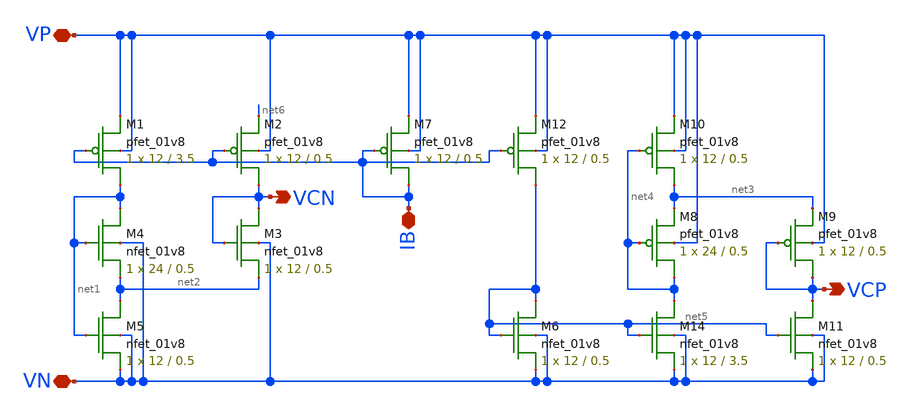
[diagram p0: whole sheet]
** sch_path: mp3/schematics/bias_generator (another copy).sch
**.subckt bias_generator (another copy) VCN VP VN VCP IB
*.opin VCN
*.iopin VP
*.iopin VN
*.opin VCP
*.iopin IB
XM1 net1 IB VP VP sky130_fd_pr__pfet_01v8 L=3.5 W=12 nf=1 ad='int((nf+1)/2) * W/nf * 0.29' as='int((nf+2)/2) * W/nf * 0.29'
+ pd='2*int((nf+1)/2) * (W/nf + 0.29)' ps='2*int((nf+2)/2) * (W/nf + 0.29)' nrd='0.29 / W' nrs='0.29 / W'
+ sa=0 sb=0 sd=0 mult=1 m=1
XM2 VCN IB net6 VP sky130_fd_pr__pfet_01v8 L=0.5 W=12 nf=1 ad='int((nf+1)/2) * W/nf * 0.29' as='int((nf+2)/2) * W/nf * 0.29'
+ pd='2*int((nf+1)/2) * (W/nf + 0.29)' ps='2*int((nf+2)/2) * (W/nf + 0.29)' nrd='0.29 / W' nrs='0.29 / W'
+ sa=0 sb=0 sd=0 mult=1 m=1
XM8 net4 net4 net3 VP sky130_fd_pr__pfet_01v8 L=0.5 W=24 nf=1 ad='int((nf+1)/2) * W/nf * 0.29' as='int((nf+2)/2) * W/nf * 0.29'
+ pd='2*int((nf+1)/2) * (W/nf + 0.29)' ps='2*int((nf+2)/2) * (W/nf + 0.29)' nrd='0.29 / W' nrs='0.29 / W'
+ sa=0 sb=0 sd=0 mult=1 m=1
XM9 VCP VCP net3 VP sky130_fd_pr__pfet_01v8 L=0.5 W=12 nf=1 ad='int((nf+1)/2) * W/nf * 0.29' as='int((nf+2)/2) * W/nf * 0.29'
+ pd='2*int((nf+1)/2) * (W/nf + 0.29)' ps='2*int((nf+2)/2) * (W/nf + 0.29)' nrd='0.29 / W' nrs='0.29 / W'
+ sa=0 sb=0 sd=0 mult=1 m=1
XM10 net3 net4 VP VP sky130_fd_pr__pfet_01v8 L=0.5 W=12 nf=1 ad='int((nf+1)/2) * W/nf * 0.29' as='int((nf+2)/2) * W/nf * 0.29'
+ pd='2*int((nf+1)/2) * (W/nf + 0.29)' ps='2*int((nf+2)/2) * (W/nf + 0.29)' nrd='0.29 / W' nrs='0.29 / W'
+ sa=0 sb=0 sd=0 mult=1 m=1
XM11 VCP net5 VN VN sky130_fd_pr__nfet_01v8 L=0.5 W=12 nf=1 ad='int((nf+1)/2) * W/nf * 0.29' as='int((nf+2)/2) * W/nf * 0.29'
+ pd='2*int((nf+1)/2) * (W/nf + 0.29)' ps='2*int((nf+2)/2) * (W/nf + 0.29)' nrd='0.29 / W' nrs='0.29 / W'
+ sa=0 sb=0 sd=0 mult=1 m=1
XM14 net4 net5 VN VN sky130_fd_pr__nfet_01v8 L=3.5 W=12 nf=1 ad='int((nf+1)/2) * W/nf * 0.29' as='int((nf+2)/2) * W/nf * 0.29'
+ pd='2*int((nf+1)/2) * (W/nf + 0.29)' ps='2*int((nf+2)/2) * (W/nf + 0.29)' nrd='0.29 / W' nrs='0.29 / W'
+ sa=0 sb=0 sd=0 mult=1 m=1
XM6 net5 net5 VN VN sky130_fd_pr__nfet_01v8 L=0.5 W=12 nf=1 ad='int((nf+1)/2) * W/nf * 0.29' as='int((nf+2)/2) * W/nf * 0.29'
+ pd='2*int((nf+1)/2) * (W/nf + 0.29)' ps='2*int((nf+2)/2) * (W/nf + 0.29)' nrd='0.29 / W' nrs='0.29 / W'
+ sa=0 sb=0 sd=0 mult=1 m=1
XM3 VCN VCN net2 VN sky130_fd_pr__nfet_01v8 L=0.5 W=12 nf=1 ad='int((nf+1)/2) * W/nf * 0.29' as='int((nf+2)/2) * W/nf * 0.29'
+ pd='2*int((nf+1)/2) * (W/nf + 0.29)' ps='2*int((nf+2)/2) * (W/nf + 0.29)' nrd='0.29 / W' nrs='0.29 / W'
+ sa=0 sb=0 sd=0 mult=1 m=1
XM4 net1 net1 net2 VN sky130_fd_pr__nfet_01v8 L=0.5 W=24 nf=1 ad='int((nf+1)/2) * W/nf * 0.29' as='int((nf+2)/2) * W/nf * 0.29'
+ pd='2*int((nf+1)/2) * (W/nf + 0.29)' ps='2*int((nf+2)/2) * (W/nf + 0.29)' nrd='0.29 / W' nrs='0.29 / W'
+ sa=0 sb=0 sd=0 mult=1 m=1
XM5 net2 net1 VN VN sky130_fd_pr__nfet_01v8 L=0.5 W=12 nf=1 ad='int((nf+1)/2) * W/nf * 0.29' as='int((nf+2)/2) * W/nf * 0.29'
+ pd='2*int((nf+1)/2) * (W/nf + 0.29)' ps='2*int((nf+2)/2) * (W/nf + 0.29)' nrd='0.29 / W' nrs='0.29 / W'
+ sa=0 sb=0 sd=0 mult=1 m=1
XM12 net5 IB VP VP sky130_fd_pr__pfet_01v8 L=0.5 W=12 nf=1 ad='int((nf+1)/2) * W/nf * 0.29' as='int((nf+2)/2) * W/nf * 0.29'
+ pd='2*int((nf+1)/2) * (W/nf + 0.29)' ps='2*int((nf+2)/2) * (W/nf + 0.29)' nrd='0.29 / W' nrs='0.29 / W'
+ sa=0 sb=0 sd=0 mult=1 m=1
XM7 IB IB VP VP sky130_fd_pr__pfet_01v8 L=0.5 W=12 nf=1 ad='int((nf+1)/2) * W/nf * 0.29' as='int((nf+2)/2) * W/nf * 0.29'
+ pd='2*int((nf+1)/2) * (W/nf + 0.29)' ps='2*int((nf+2)/2) * (W/nf + 0.29)' nrd='0.29 / W' nrs='0.29 / W'
+ sa=0 sb=0 sd=0 mult=1 m=1
**.ends
.end
